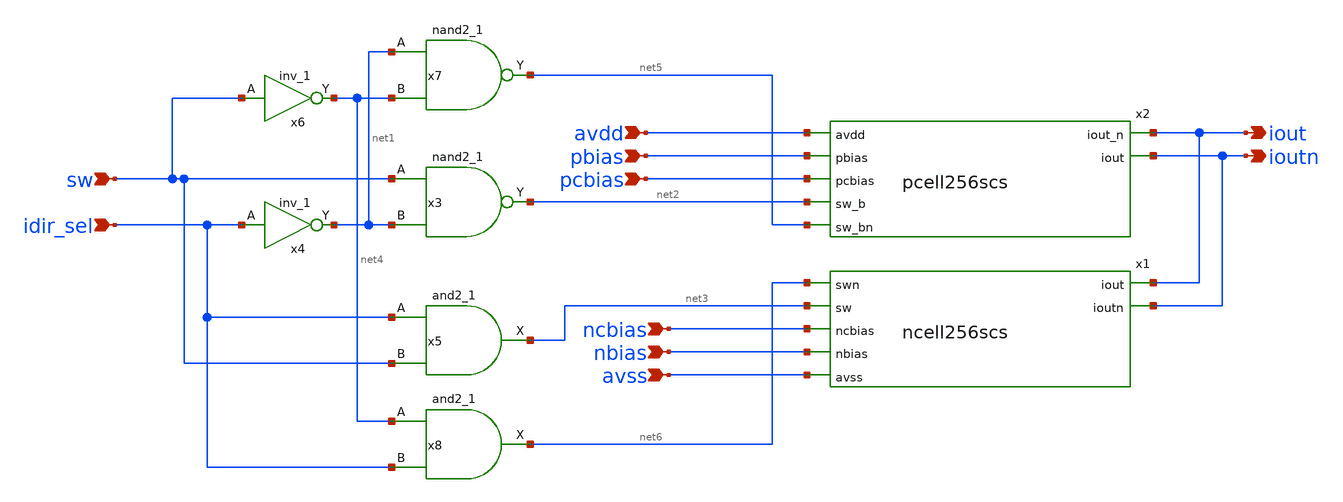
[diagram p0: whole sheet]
** sch_path: xschem/icell256_unary_scs.sch
**.subckt icell256_unary_scs avdd pbias pcbias sw idir_sel ncbias nbias avss iout ioutn
*.ipin avdd
*.ipin pbias
*.ipin pcbias
*.ipin sw
*.ipin idir_sel
*.ipin ncbias
*.ipin nbias
*.ipin avss
*.opin iout
*.opin ioutn
x3 sw net1 avss avss avdd avdd net2 sky130_fd_sc_hvl__nand2_1
x5 idir_sel sw avss avss avdd avdd net3 sky130_fd_sc_hvl__and2_1
x4 idir_sel avss avss avdd avdd net1 sky130_fd_sc_hvl__inv_1
x6 sw avss avss avdd avdd net4 sky130_fd_sc_hvl__inv_1
x7 net1 net4 avss avss avdd avdd net5 sky130_fd_sc_hvl__nand2_1
x8 net4 idir_sel avss avss avdd avdd net6 sky130_fd_sc_hvl__and2_1
x1 iout ioutn net6 net3 ncbias nbias avss ncell256scs
x2 avdd pbias pcbias net2 net5 iout ioutn pcell256scs
**.ends

* expanding   symbol:  ncell256scs.sym # of pins=7
** sym_path: xschem/ncell256scs.sym
** sch_path: xschem/ncell256scs.sch
.subckt ncell256scs iout ioutn swn sw ncbias nbias avss
*.ipin sw
*.ipin ncbias
*.ipin nbias
*.ipin avss
*.opin iout
*.opin ioutn
*.ipin swn
XM8 net1 nbias avss avss sky130_fd_pr__nfet_g5v0d10v5 L=0.5 W=3 nf=1 ad='int((nf+1)/2) * W/nf * 0.29'
+ as='int((nf+2)/2) * W/nf * 0.29' pd='2*int((nf+1)/2) * (W/nf + 0.29)' ps='2*int((nf+2)/2) * (W/nf + 0.29)'
+ nrd='0.29 / W' nrs='0.29 / W' sa=0 sb=0 sd=0 mult=256 m=256
XM9 net2 ncbias net1 avss sky130_fd_pr__nfet_g5v0d10v5 L=0.5 W=6 nf=1 ad='int((nf+1)/2) * W/nf * 0.29'
+ as='int((nf+2)/2) * W/nf * 0.29' pd='2*int((nf+1)/2) * (W/nf + 0.29)' ps='2*int((nf+2)/2) * (W/nf + 0.29)'
+ nrd='0.29 / W' nrs='0.29 / W' sa=0 sb=0 sd=0 mult=256 m=256
XM1 iout sw net2 avss sky130_fd_pr__nfet_g5v0d10v5 L=0.5 W=6 nf=1 ad='int((nf+1)/2) * W/nf * 0.29' as='int((nf+2)/2) * W/nf * 0.29'
+ pd='2*int((nf+1)/2) * (W/nf + 0.29)' ps='2*int((nf+2)/2) * (W/nf + 0.29)' nrd='0.29 / W' nrs='0.29 / W'
+ sa=0 sb=0 sd=0 mult=256 m=256
XM2 ioutn swn net2 avss sky130_fd_pr__nfet_g5v0d10v5 L=0.5 W=6 nf=1 ad='int((nf+1)/2) * W/nf * 0.29'
+ as='int((nf+2)/2) * W/nf * 0.29' pd='2*int((nf+1)/2) * (W/nf + 0.29)' ps='2*int((nf+2)/2) * (W/nf + 0.29)'
+ nrd='0.29 / W' nrs='0.29 / W' sa=0 sb=0 sd=0 mult=256 m=256
.ends


* expanding   symbol:  pcell256scs.sym # of pins=7
** sym_path: xschem/pcell256scs.sym
** sch_path: xschem/pcell256scs.sch
.subckt pcell256scs avdd pbias pcbias sw_b sw_bn iout_n iout
*.ipin pbias
*.ipin pcbias
*.ipin sw_b
*.ipin avdd
*.opin iout
*.opin iout_n
*.ipin sw_bn
XM1 net1 pbias avdd avdd sky130_fd_pr__pfet_g5v0d10v5 L=0.5 W=6 nf=1 ad='int((nf+1)/2) * W/nf * 0.29'
+ as='int((nf+2)/2) * W/nf * 0.29' pd='2*int((nf+1)/2) * (W/nf + 0.29)' ps='2*int((nf+2)/2) * (W/nf + 0.29)'
+ nrd='0.29 / W' nrs='0.29 / W' sa=0 sb=0 sd=0 mult=256 m=256
XM2 net2 pcbias net1 avdd sky130_fd_pr__pfet_g5v0d10v5 L=0.5 W=12 nf=1 ad='int((nf+1)/2) * W/nf * 0.29'
+ as='int((nf+2)/2) * W/nf * 0.29' pd='2*int((nf+1)/2) * (W/nf + 0.29)' ps='2*int((nf+2)/2) * (W/nf + 0.29)'
+ nrd='0.29 / W' nrs='0.29 / W' sa=0 sb=0 sd=0 mult=256 m=256
XM3 iout sw_b net2 avdd sky130_fd_pr__pfet_g5v0d10v5 L=0.5 W=4 nf=1 ad='int((nf+1)/2) * W/nf * 0.29'
+ as='int((nf+2)/2) * W/nf * 0.29' pd='2*int((nf+1)/2) * (W/nf + 0.29)' ps='2*int((nf+2)/2) * (W/nf + 0.29)'
+ nrd='0.29 / W' nrs='0.29 / W' sa=0 sb=0 sd=0 mult=256 m=256
XM4 iout_n sw_bn net2 avdd sky130_fd_pr__pfet_g5v0d10v5 L=0.5 W=4 nf=1 ad='int((nf+1)/2) * W/nf * 0.29'
+ as='int((nf+2)/2) * W/nf * 0.29' pd='2*int((nf+1)/2) * (W/nf + 0.29)' ps='2*int((nf+2)/2) * (W/nf + 0.29)'
+ nrd='0.29 / W' nrs='0.29 / W' sa=0 sb=0 sd=0 mult=256 m=256
.ends

.end
